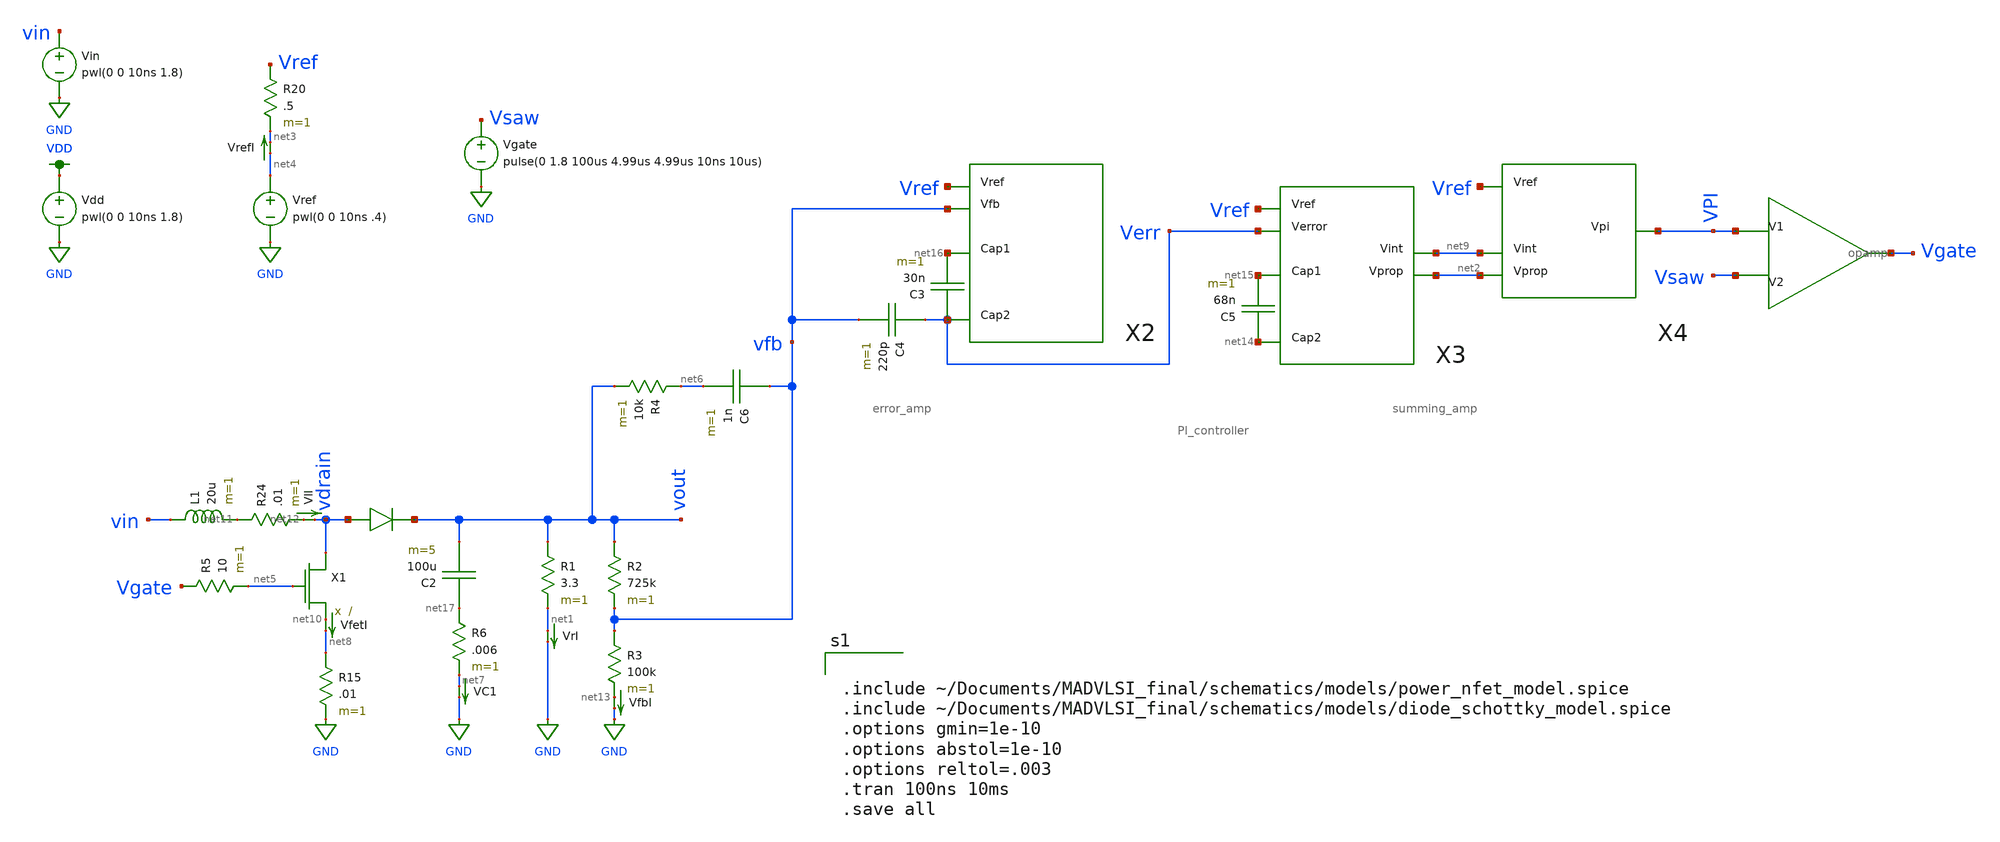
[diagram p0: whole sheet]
** sch_path: schematics/boost_VMC_tmp.sch
**.subckt boost_VMC_tmp
Vin vin GND pwl(0 0 10ns 1.8)
VfetI net10 net8 0
.save i(vfeti)
X1 vdrain net5 net10 power_nfet
L1 vin net11 20u m=1
D1 vdrain vout diode_schottky
R1 vout net1 3.3 m=1
VlI net12 vdrain 0
.save i(vli)
VrI net1 GND 0
.save i(vri)
R2 vout vfb 725k m=1
R3 vfb net13 100k m=1
Vdd VDD GND pwl(0 0 10ns 1.8)
Vref net4 GND pwl(0 0 10ns .4)
C5 net14 net15 68n m=1
X11 VPI Vsaw Vgate opamp
Vgate Vsaw GND pulse(0 1.8 100us 4.99us 4.99us 10ns 10us)
VrefI net4 net3 0
.save i(vrefi)
R24 net11 net12 .01 m=1
VfbI net13 GND 0
.save i(vfbi)
R20 Vref net3 .5 m=1
C3 Verr net16 30n m=1
C4 Verr vfb 220p m=1
R4 net6 vout 10k m=1
C6 vfb net6 1n m=1
R5 Vgate net5 10 m=1
C2 net17 vout 100u m=5
R6 net17 net7 .006 m=1
VC1 net7 GND 0
.save i(vc1)
R15 net8 GND .01 m=1
X2 Vref net16 vfb Verr error_amp
X3 Vref net15 Verr net14 net9 net2 PI_controller
X4 Vref VPI net9 net2 summing_amp
**** begin user architecture code


.include ~/Documents/MADVLSI_final/schematics/models/power_nfet_model.spice
.include ~/Documents/MADVLSI_final/schematics/models/diode_schottky_model.spice
.options gmin=1e-10
.options abstol=1e-10
.options reltol=.003
.tran 100ns 10ms
.save all


.option wnflag=1
.lib ~/skywater/skywater-pdk/libraries/sky130_fd_pr_ngspice/latest/models/sky130.lib.spice tt

**** end user architecture code
**.ends
.GLOBAL GND
.GLOBAL VDD
.end
